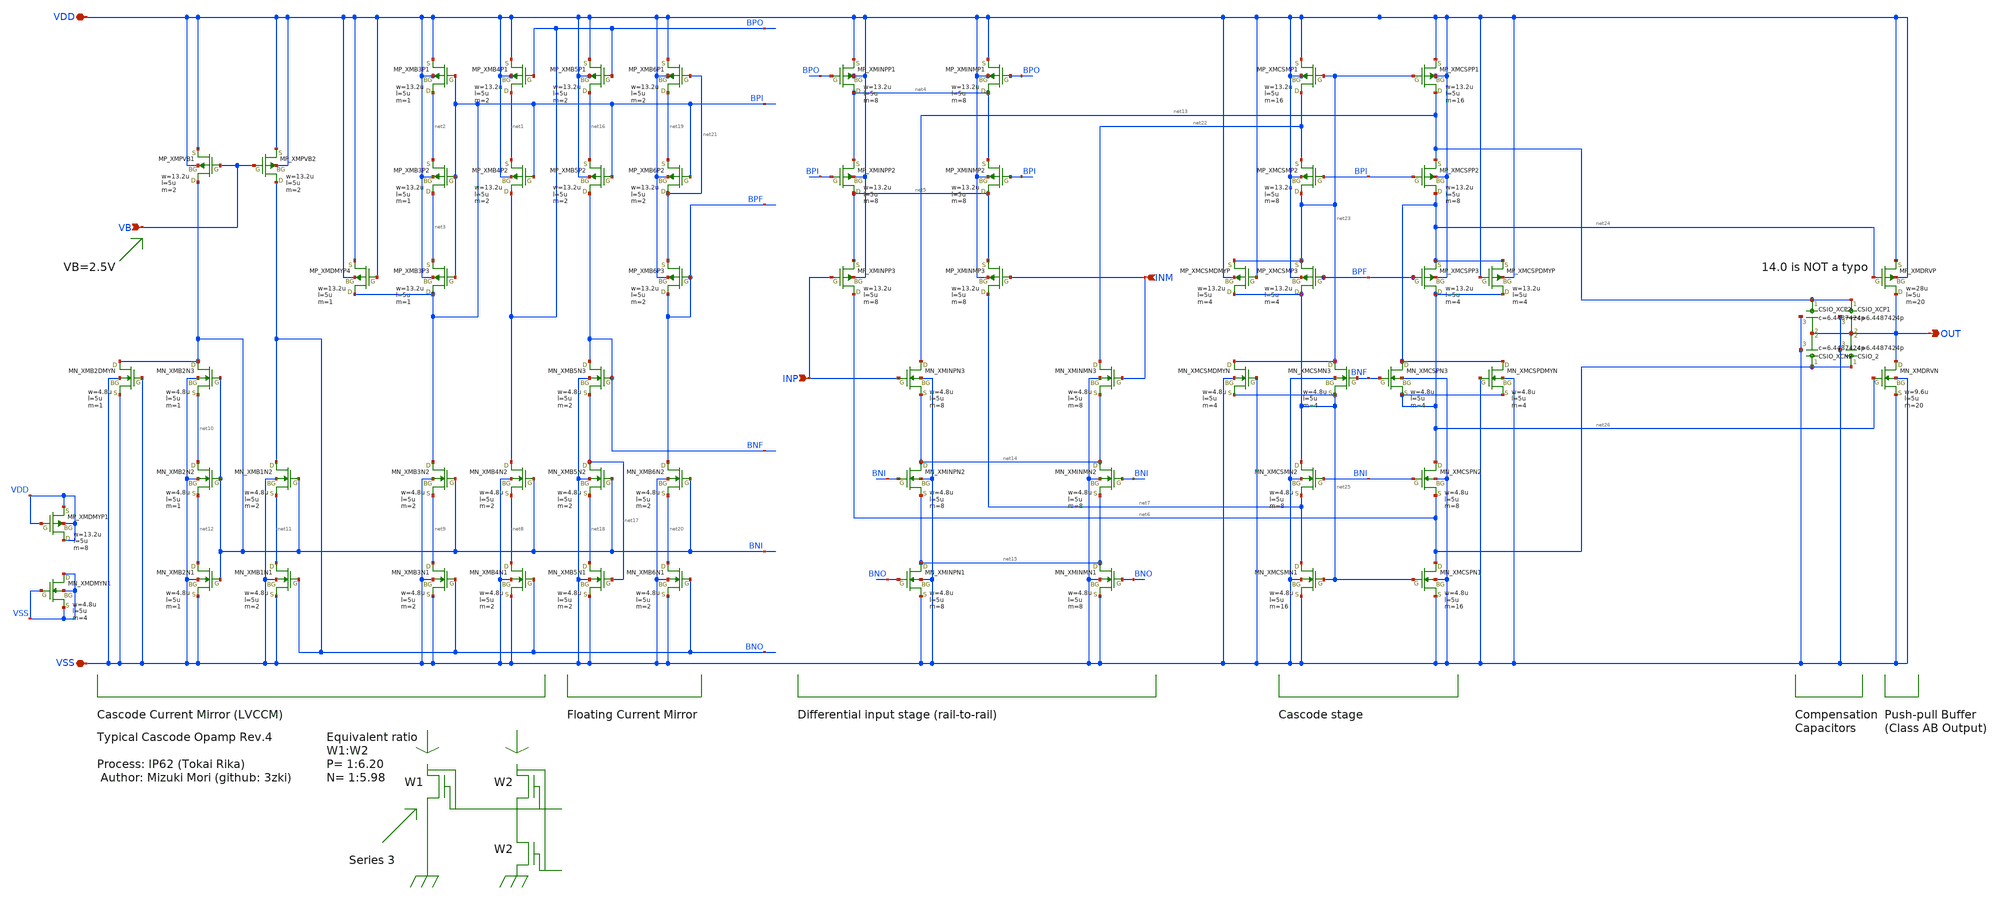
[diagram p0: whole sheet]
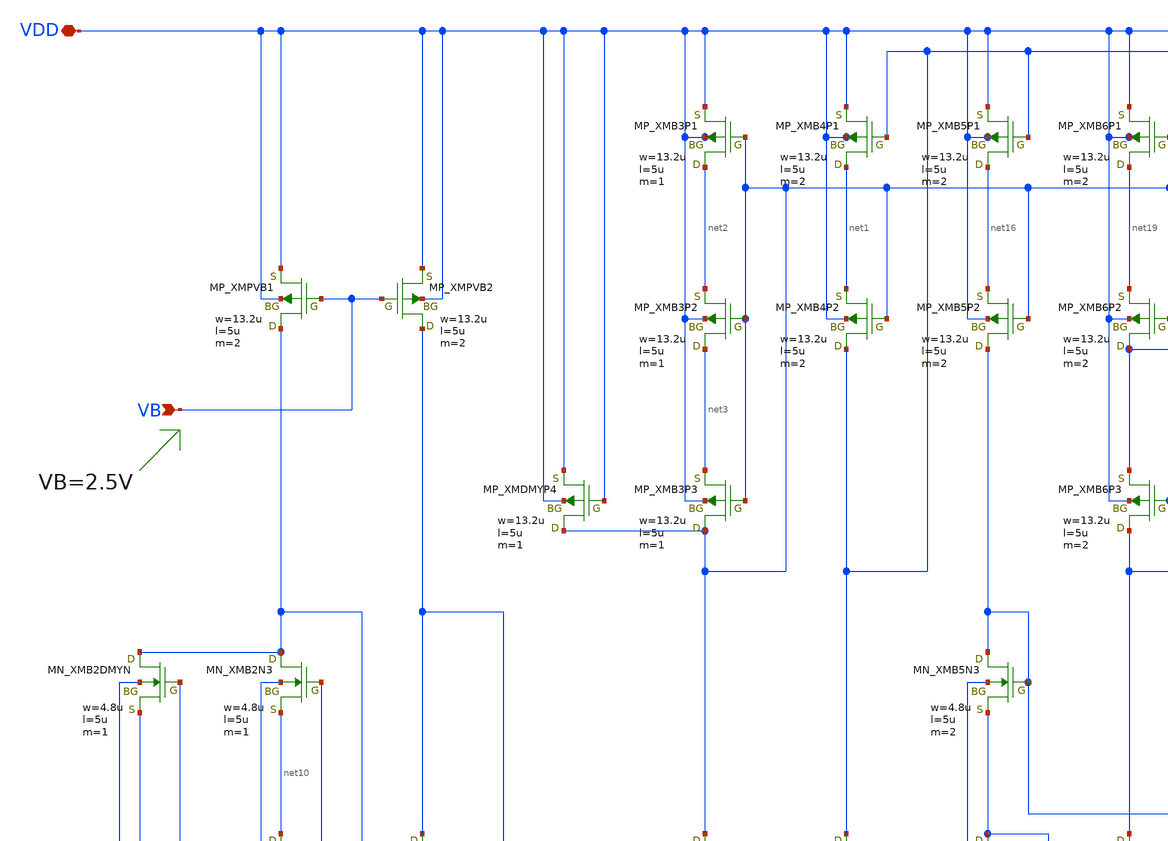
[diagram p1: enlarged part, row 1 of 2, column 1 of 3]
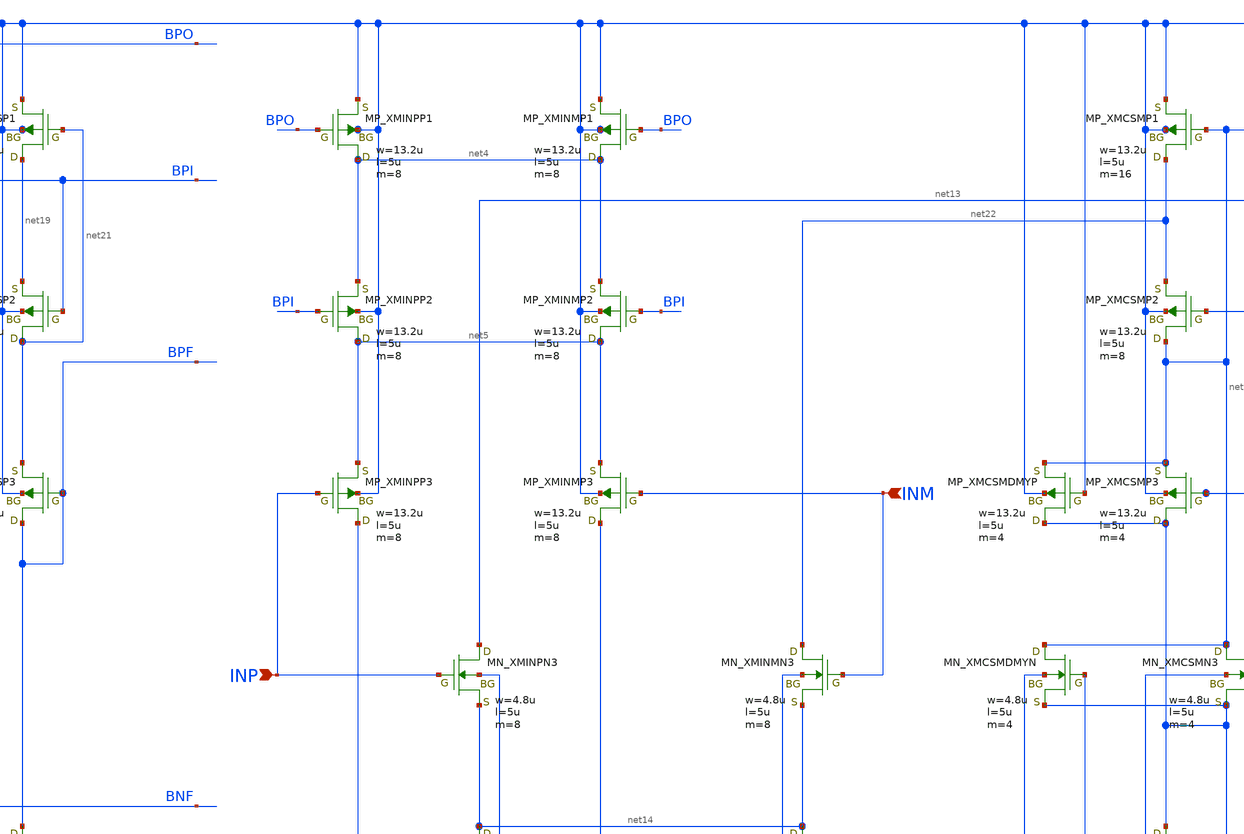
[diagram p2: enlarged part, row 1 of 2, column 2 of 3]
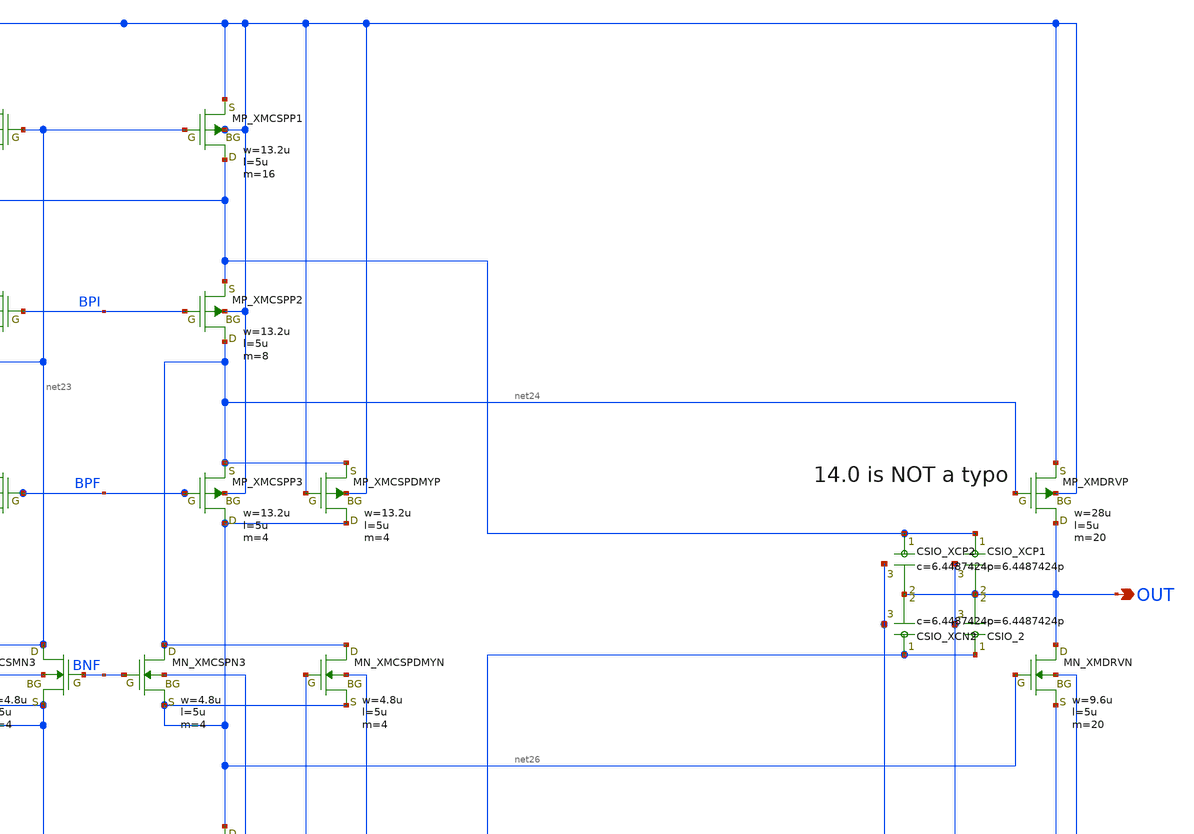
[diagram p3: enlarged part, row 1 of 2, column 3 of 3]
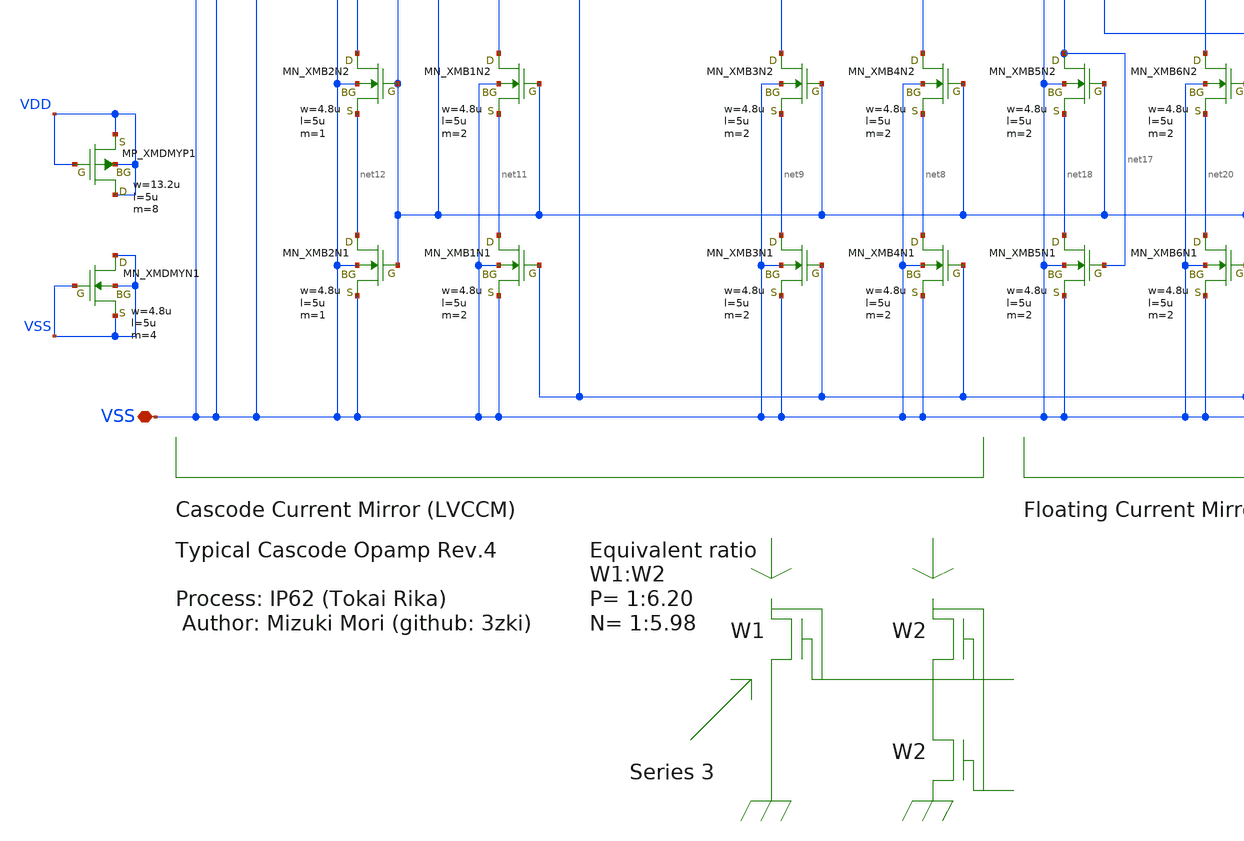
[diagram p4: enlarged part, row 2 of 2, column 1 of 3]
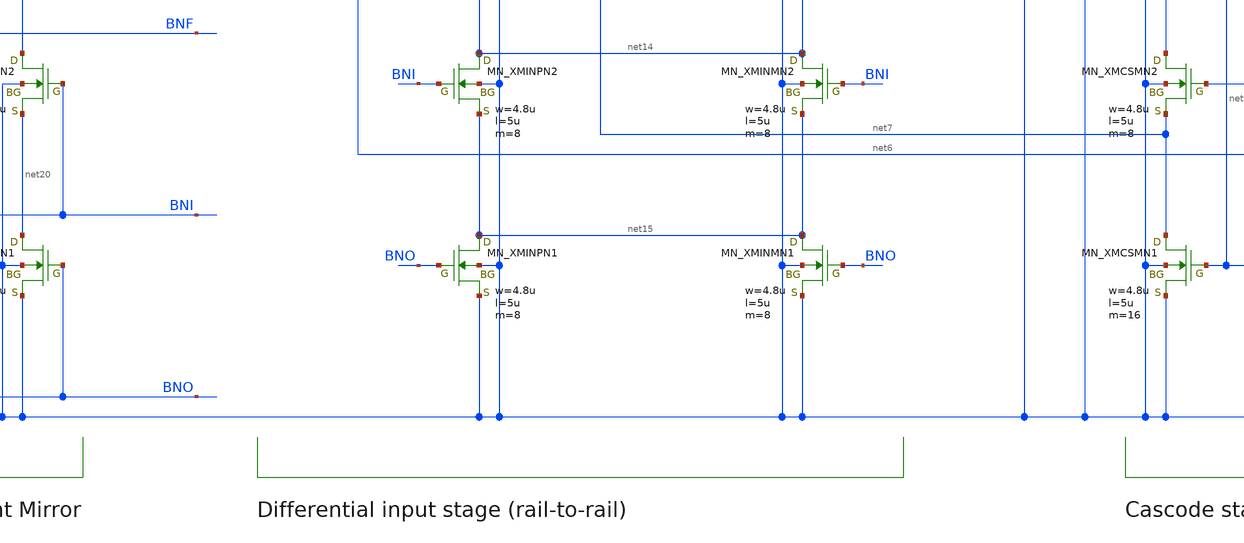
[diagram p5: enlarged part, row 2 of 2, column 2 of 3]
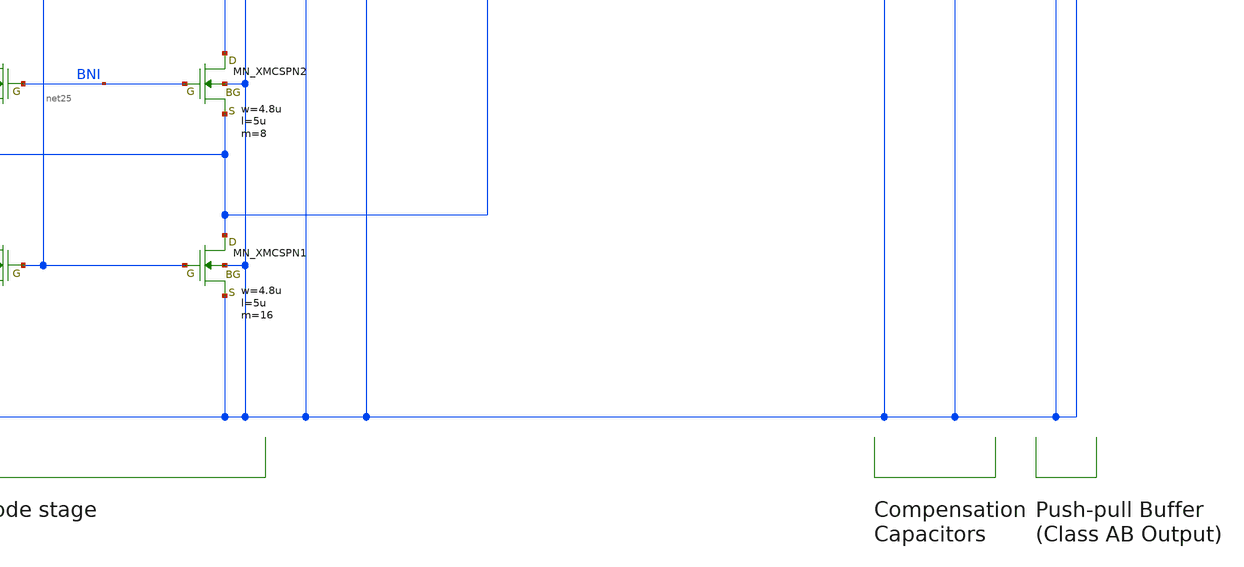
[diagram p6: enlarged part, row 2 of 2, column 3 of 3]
** sch_path: member_project/opamp_r2r_audio/3zki/opamp_3zki_R06_2V5_FULL.sch
**.subckt opamp_3zki_R06_2V5_FULL VDD VSS INP INM OUT VB
*.iopin VDD
*.iopin VSS
*.ipin INP
*.ipin INM
*.opin OUT
*.ipin VB
XMDRVP OUT net24 VDD VDD PMOS w=28u l=5u as=21p ad=21p ps=17u pd=17u nrd=0 nrs=0 m=20
XMDRVN OUT net26 VSS VSS NMOS w=9.6u l=5u as=7.2p ad=7.2p ps=7.8u pd=7.8u nrd=0 nrs=0 m=20
XMB4P1 net1 BPO VDD VDD PMOS w=13.2u l=5u as=19.8p ad=19.8p ps=16.2u pd=16.2u nrd=0 nrs=0 m=2
XMB4P2 BPO BPI net1 VDD PMOS w=13.2u l=5u as=19.8p ad=19.8p ps=16.2u pd=16.2u nrd=0 nrs=0 m=2
XMB3P1 net2 BPI VDD VDD PMOS w=13.2u l=5u as=19.8p ad=19.8p ps=16.2u pd=16.2u nrd=0 nrs=0 m=1
XMB3P2 net3 BPI net2 VDD PMOS w=13.2u l=5u as=19.8p ad=19.8p ps=16.2u pd=16.2u nrd=0 nrs=0 m=1
XMB3P3 BPI BPI net3 VDD PMOS w=13.2u l=5u as=19.8p ad=19.8p ps=16.2u pd=16.2u nrd=0 nrs=0 m=1
XMINPP1 net4 BPO VDD VDD PMOS w=13.2u l=5u as=20.4p ad=20.4p ps=16.6u pd=16.6u nrd=0 nrs=0 m=8
XMINPP2 net5 BPI net4 VDD PMOS w=13.2u l=5u as=20.4p ad=20.4p ps=16.6u pd=16.6u nrd=0 nrs=0 m=8
XMINPP3 net6 INP net5 VDD PMOS w=13.2u l=5u as=20.4p ad=20.4p ps=16.6u pd=16.6u nrd=0 nrs=0 m=8
XMINMP1 net4 BPO VDD VDD PMOS w=13.2u l=5u as=20.4p ad=20.4p ps=16.6u pd=16.6u nrd=0 nrs=0 m=8
XMINMP2 net5 BPI net4 VDD PMOS w=13.2u l=5u as=20.4p ad=20.4p ps=16.6u pd=16.6u nrd=0 nrs=0 m=8
XMINMP3 net7 INM net5 VDD PMOS w=13.2u l=5u as=20.4p ad=20.4p ps=16.6u pd=16.6u nrd=0 nrs=0 m=8
XMB4N2 BPO BNI net8 VSS NMOS w=4.8u l=5u as=7.2p ad=7.2p ps=7.8u pd=7.8u nrd=0 nrs=0 m=2
XMB3N2 BPI BNI net9 VSS NMOS w=4.8u l=5u as=7.2p ad=7.2p ps=7.8u pd=7.8u nrd=0 nrs=0 m=2
XMB4N1 net8 BNO VSS VSS NMOS w=4.8u l=5u as=7.2p ad=7.2p ps=7.8u pd=7.8u nrd=0 nrs=0 m=2
XMB3N1 net9 BNO VSS VSS NMOS w=4.8u l=5u as=7.2p ad=7.2p ps=7.8u pd=7.8u nrd=0 nrs=0 m=2
XMB1N2 BNO BNI net11 VSS NMOS w=4.8u l=5u as=7.2p ad=7.2p ps=7.8u pd=7.8u nrd=0 nrs=0 m=2
XMB2N2 net10 BNI net12 VSS NMOS w=4.8u l=5u as=7.2p ad=7.2p ps=7.8u pd=7.8u nrd=0 nrs=0 m=1
XMB1N1 net11 BNO VSS VSS NMOS w=4.8u l=5u as=7.2p ad=7.2p ps=7.8u pd=7.8u nrd=0 nrs=0 m=2
XMB2N1 net12 BNI VSS VSS NMOS w=4.8u l=5u as=7.2p ad=7.2p ps=7.8u pd=7.8u nrd=0 nrs=0 m=1
XMB2N3 BNI BNI net10 VSS NMOS w=4.8u l=5u as=7.2p ad=7.2p ps=7.8u pd=7.8u nrd=0 nrs=0 m=1
XMINPN2 net14 BNI net15 VSS NMOS w=4.8u l=5u as=7.2p ad=7.2p ps=7.8u pd=7.8u nrd=0 nrs=0 m=8
XMINPN1 net15 BNO VSS VSS NMOS w=4.8u l=5u as=7.2p ad=7.2p ps=7.8u pd=7.8u nrd=0 nrs=0 m=8
XMINPN3 net13 INP net14 VSS NMOS w=4.8u l=5u as=7.2p ad=7.2p ps=7.8u pd=7.8u nrd=0 nrs=0 m=8
XMB5P1 net16 BPO VDD VDD PMOS w=13.2u l=5u as=19.8p ad=19.8p ps=16.2u pd=16.2u nrd=0 nrs=0 m=2
XMB5P2 BNF BPI net16 VDD PMOS w=13.2u l=5u as=19.8p ad=19.8p ps=16.2u pd=16.2u nrd=0 nrs=0 m=2
XMB5N2 net17 BNI net18 VSS NMOS w=4.8u l=5u as=7.2p ad=7.2p ps=7.8u pd=7.8u nrd=0 nrs=0 m=2
XMB5N1 net18 net17 VSS VSS NMOS w=4.8u l=5u as=7.2p ad=7.2p ps=7.8u pd=7.8u nrd=0 nrs=0 m=2
XMB5N3 BNF BNF net17 VSS NMOS w=4.8u l=5u as=7.2p ad=7.2p ps=7.8u pd=7.8u nrd=0 nrs=0 m=2
XMB6P1 net19 net21 VDD VDD PMOS w=13.2u l=5u as=19.8p ad=19.8p ps=16.2u pd=16.2u nrd=0 nrs=0 m=2
XMB6P2 net21 BPI net19 VDD PMOS w=13.2u l=5u as=19.8p ad=19.8p ps=16.2u pd=16.2u nrd=0 nrs=0 m=2
XMB6N2 BPF BNI net20 VSS NMOS w=4.8u l=5u as=7.2p ad=7.2p ps=7.8u pd=7.8u nrd=0 nrs=0 m=2
XMB6N1 net20 BNO VSS VSS NMOS w=4.8u l=5u as=7.2p ad=7.2p ps=7.8u pd=7.8u nrd=0 nrs=0 m=2
XMB6P3 BPF BPF net21 VDD PMOS w=13.2u l=5u as=19.8p ad=19.8p ps=16.2u pd=16.2u nrd=0 nrs=0 m=2
XMB2DMYN BNI VSS VSS VSS NMOS w=4.8u l=5u as=7.2p ad=7.2p ps=7.8u pd=7.8u nrd=0 nrs=0 m=1
XMINMN2 net14 BNI net15 VSS NMOS w=4.8u l=5u as=7.2p ad=7.2p ps=7.8u pd=7.8u nrd=0 nrs=0 m=8
XMINMN1 net15 BNO VSS VSS NMOS w=4.8u l=5u as=7.2p ad=7.2p ps=7.8u pd=7.8u nrd=0 nrs=0 m=8
XMINMN3 net22 INM net14 VSS NMOS w=4.8u l=5u as=7.2p ad=7.2p ps=7.8u pd=7.8u nrd=0 nrs=0 m=8
XMCSMP1 net22 net23 VDD VDD PMOS w=13.2u l=5u as=19.8p ad=19.8p ps=16.2u pd=16.2u nrd=0 nrs=0 m=16
XMCSMP2 net23 BPI net22 VDD PMOS w=13.2u l=5u as=19.8p ad=19.8p ps=16.2u pd=16.2u nrd=0 nrs=0 m=8
XMCSMP3 net25 BPF net23 VDD PMOS w=13.2u l=5u as=19.8p ad=19.8p ps=16.2u pd=16.2u nrd=0 nrs=0 m=4
XMCSPP1 net13 net23 VDD VDD PMOS w=13.2u l=5u as=19.8p ad=19.8p ps=16.2u pd=16.2u nrd=0 nrs=0 m=16
XMCSPP2 net24 BPI net13 VDD PMOS w=13.2u l=5u as=19.8p ad=19.8p ps=16.2u pd=16.2u nrd=0 nrs=0 m=8
XMCSPP3 net26 BPF net24 VDD PMOS w=13.2u l=5u as=19.8p ad=19.8p ps=16.2u pd=16.2u nrd=0 nrs=0 m=4
XMCSMN2 net25 BNI net7 VSS NMOS w=4.8u l=5u as=7.2p ad=7.2p ps=7.8u pd=7.8u nrd=0 nrs=0 m=8
XMCSMN1 net7 net25 VSS VSS NMOS w=4.8u l=5u as=7.2p ad=7.2p ps=7.8u pd=7.8u nrd=0 nrs=0 m=16
XMCSMN3 net23 BNF net25 VSS NMOS w=4.8u l=5u as=7.2p ad=7.2p ps=7.8u pd=7.8u nrd=0 nrs=0 m=4
XMCSPN3 net24 BNF net26 VSS NMOS w=4.8u l=5u as=7.2p ad=7.2p ps=7.8u pd=7.8u nrd=0 nrs=0 m=4
XMCSPN2 net26 BNI net6 VSS NMOS w=4.8u l=5u as=7.2p ad=7.2p ps=7.8u pd=7.8u nrd=0 nrs=0 m=8
XMCSPN1 net6 net25 VSS VSS NMOS w=4.8u l=5u as=7.2p ad=7.2p ps=7.8u pd=7.8u nrd=0 nrs=0 m=16
XCP1 net13 OUT VSS F_CSIO c=6.4487424p x=120u y=87.3u m=1
XCP2 net13 OUT VSS F_CSIO c=6.4487424p x=120u y=87.3u m=1
2 net6 OUT VSS F_CSIO c=6.4487424p x=120u y=87.3u m=1
XCN2 net6 OUT VSS F_CSIO c=6.4487424p x=120u y=87.3u m=1
XMPVB1 BNI VB VDD VDD PMOS w=13.2u l=5u as=19.8p ad=19.8p ps=16.2u pd=16.2u nrd=0 nrs=0 m=2
XMPVB2 BNO VB VDD VDD PMOS w=13.2u l=5u as=19.8p ad=19.8p ps=16.2u pd=16.2u nrd=0 nrs=0 m=2
XMDMYP4 BPI VDD VDD VDD PMOS w=13.2u l=5u as=19.8p ad=19.8p ps=16.2u pd=16.2u nrd=0 nrs=0 m=1
XMCSMDMYP net25 VDD net23 VDD PMOS w=13.2u l=5u as=19.8p ad=19.8p ps=16.2u pd=16.2u nrd=0 nrs=0 m=4
XMCSPDMYP net26 VDD net24 VDD PMOS w=13.2u l=5u as=19.8p ad=19.8p ps=16.2u pd=16.2u nrd=0 nrs=0 m=4
XMCSMDMYN net23 VSS net25 VSS NMOS w=4.8u l=5u as=7.2p ad=7.2p ps=7.8u pd=7.8u nrd=0 nrs=0 m=4
XMCSPDMYN net24 VSS net26 VSS NMOS w=4.8u l=5u as=7.2p ad=7.2p ps=7.8u pd=7.8u nrd=0 nrs=0 m=4
XMDMYN1 VSS VSS VSS VSS NMOS w=4.8u l=5u as=7.2p ad=7.2p ps=7.8u pd=7.8u nrd=0 nrs=0 m=4
XMDMYP1 VDD VDD VDD VDD PMOS w=13.2u l=5u as=19.8p ad=19.8p ps=16.2u pd=16.2u nrd=0 nrs=0 m=8
**.ends
.end
